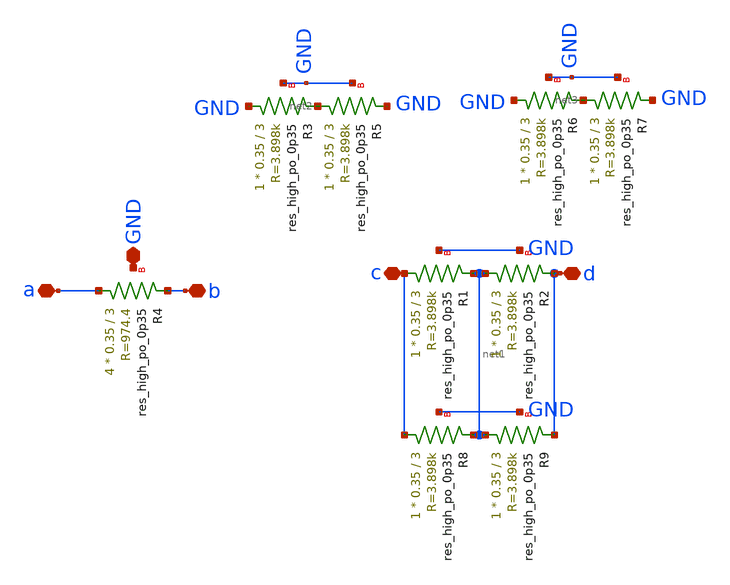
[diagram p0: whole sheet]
** sch_path: magic/resistor_op_tt.sch
**.subckt resistor_op_tt GND c d a b
*.iopin GND
*.iopin c
*.iopin d
*.iopin a
*.iopin b
XR4 a b GND sky130_fd_pr__res_high_po_0p35 L=3 mult=4 m=4
XR1 c net1 GND sky130_fd_pr__res_high_po_0p35 L=3 mult=1 m=1
XR2 net1 d GND sky130_fd_pr__res_high_po_0p35 L=3 mult=1 m=1
XR3 GND net2 GND sky130_fd_pr__res_high_po_0p35 L=3 mult=1 m=1
XR5 net2 GND GND sky130_fd_pr__res_high_po_0p35 L=3 mult=1 m=1
XR6 GND net3 GND sky130_fd_pr__res_high_po_0p35 L=3 mult=1 m=1
XR7 net3 GND GND sky130_fd_pr__res_high_po_0p35 L=3 mult=1 m=1
XR8 c net1 GND sky130_fd_pr__res_high_po_0p35 L=3 mult=1 m=1
XR9 net1 d GND sky130_fd_pr__res_high_po_0p35 L=3 mult=1 m=1
**.ends
.end
